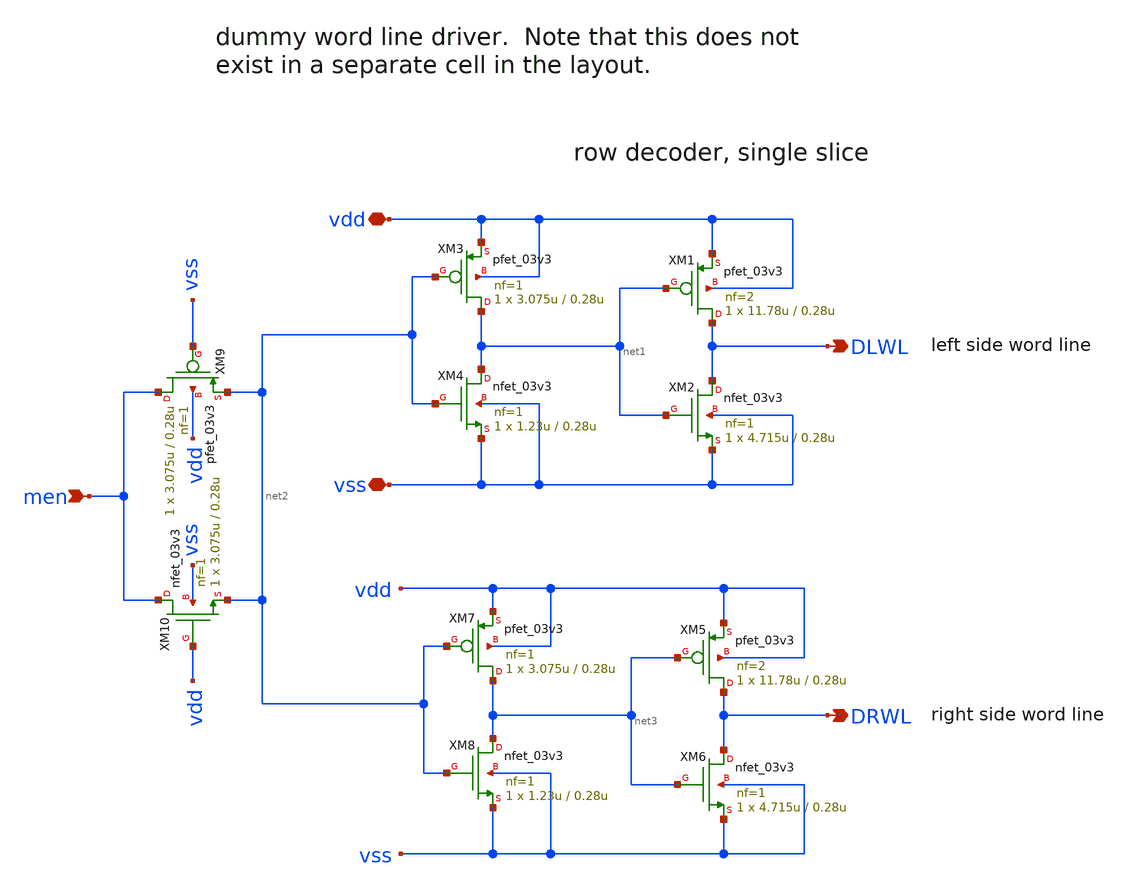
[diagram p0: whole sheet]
** sch_path: cells/gf180mcu_ocd_ip_sram__sram256x8m8wm1/xschem/ddec_3v256x8m81.sch
**.subckt ddec_3v256x8m81 DLWL DRWL men vdd vss
*.opin DLWL
*.opin DRWL
*.ipin men
*.iopin vdd
*.iopin vss
XM1 DLWL net1 vdd vdd pfet_03v3 L=0.28u W=11.78u nf=2 ad='int((nf+1)/2) * W/nf * 0.18u' as='int((nf+2)/2) * W/nf * 0.18u'
+ pd='2*int((nf+1)/2) * (W/nf + 0.18u)' ps='2*int((nf+2)/2) * (W/nf + 0.18u)' nrd='0.18u / W' nrs='0.18u / W'
+ sa=0 sb=0 sd=0 m=1
XM2 DLWL net1 vss vss nfet_03v3 L=0.28u W=4.715u nf=1 ad='int((nf+1)/2) * W/nf * 0.18u' as='int((nf+2)/2) * W/nf * 0.18u'
+ pd='2*int((nf+1)/2) * (W/nf + 0.18u)' ps='2*int((nf+2)/2) * (W/nf + 0.18u)' nrd='0.18u / W' nrs='0.18u / W'
+ sa=0 sb=0 sd=0 m=1
XM3 net1 net2 vdd vdd pfet_03v3 L=0.28u W=3.075u nf=1 ad='int((nf+1)/2) * W/nf * 0.18u' as='int((nf+2)/2) * W/nf * 0.18u'
+ pd='2*int((nf+1)/2) * (W/nf + 0.18u)' ps='2*int((nf+2)/2) * (W/nf + 0.18u)' nrd='0.18u / W' nrs='0.18u / W'
+ sa=0 sb=0 sd=0 m=1
XM4 net1 net2 vss vss nfet_03v3 L=0.28u W=1.23u nf=1 ad='int((nf+1)/2) * W/nf * 0.18u' as='int((nf+2)/2) * W/nf * 0.18u'
+ pd='2*int((nf+1)/2) * (W/nf + 0.18u)' ps='2*int((nf+2)/2) * (W/nf + 0.18u)' nrd='0.18u / W' nrs='0.18u / W'
+ sa=0 sb=0 sd=0 m=1
XM5 DRWL net3 vdd vdd pfet_03v3 L=0.28u W=11.78u nf=2 ad='int((nf+1)/2) * W/nf * 0.18u' as='int((nf+2)/2) * W/nf * 0.18u'
+ pd='2*int((nf+1)/2) * (W/nf + 0.18u)' ps='2*int((nf+2)/2) * (W/nf + 0.18u)' nrd='0.18u / W' nrs='0.18u / W'
+ sa=0 sb=0 sd=0 m=1
XM6 DRWL net3 vss vss nfet_03v3 L=0.28u W=4.715u nf=1 ad='int((nf+1)/2) * W/nf * 0.18u' as='int((nf+2)/2) * W/nf * 0.18u'
+ pd='2*int((nf+1)/2) * (W/nf + 0.18u)' ps='2*int((nf+2)/2) * (W/nf + 0.18u)' nrd='0.18u / W' nrs='0.18u / W'
+ sa=0 sb=0 sd=0 m=1
XM7 net3 net2 vdd vdd pfet_03v3 L=0.28u W=3.075u nf=1 ad='int((nf+1)/2) * W/nf * 0.18u' as='int((nf+2)/2) * W/nf * 0.18u'
+ pd='2*int((nf+1)/2) * (W/nf + 0.18u)' ps='2*int((nf+2)/2) * (W/nf + 0.18u)' nrd='0.18u / W' nrs='0.18u / W'
+ sa=0 sb=0 sd=0 m=1
XM8 net3 net2 vss vss nfet_03v3 L=0.28u W=1.23u nf=1 ad='int((nf+1)/2) * W/nf * 0.18u' as='int((nf+2)/2) * W/nf * 0.18u'
+ pd='2*int((nf+1)/2) * (W/nf + 0.18u)' ps='2*int((nf+2)/2) * (W/nf + 0.18u)' nrd='0.18u / W' nrs='0.18u / W'
+ sa=0 sb=0 sd=0 m=1
XM9 men vss net2 vdd pfet_03v3 L=0.28u W=3.075u nf=1 ad='int((nf+1)/2) * W/nf * 0.18u' as='int((nf+2)/2) * W/nf * 0.18u'
+ pd='2*int((nf+1)/2) * (W/nf + 0.18u)' ps='2*int((nf+2)/2) * (W/nf + 0.18u)' nrd='0.18u / W' nrs='0.18u / W'
+ sa=0 sb=0 sd=0 m=1
XM10 men vdd net2 vss nfet_03v3 L=0.28u W=3.075u nf=1 ad='int((nf+1)/2) * W/nf * 0.18u' as='int((nf+2)/2) * W/nf * 0.18u'
+ pd='2*int((nf+1)/2) * (W/nf + 0.18u)' ps='2*int((nf+2)/2) * (W/nf + 0.18u)' nrd='0.18u / W' nrs='0.18u / W'
+ sa=0 sb=0 sd=0 m=1
**.ends
.end
